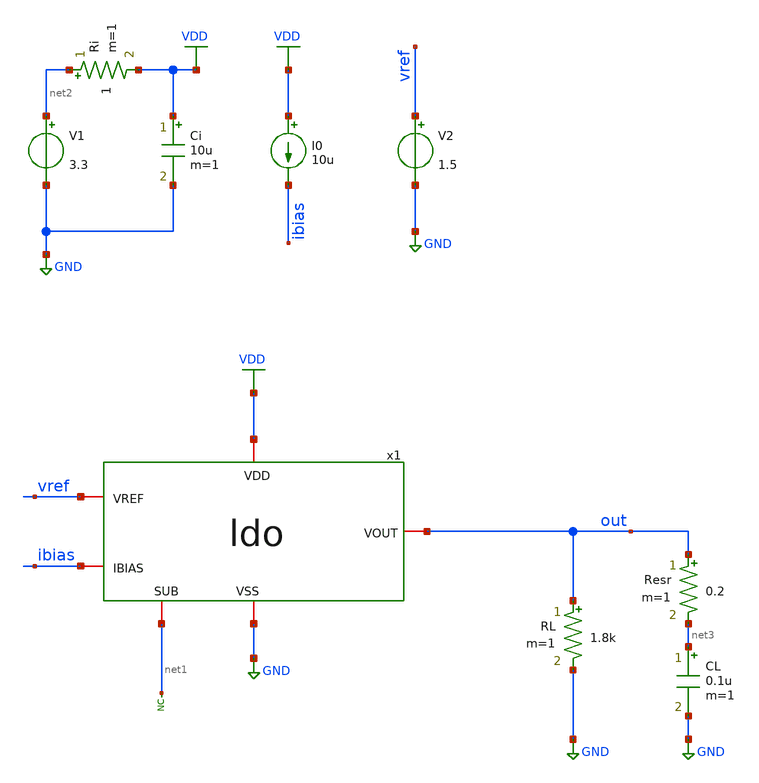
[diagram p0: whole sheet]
** sch_path: designs/libs/tb_ldo/tb_ldo/tb_ldo/tb_ldo_psrr/tb_ldo_psrr.sch
**.subckt tb_ldo_psrr
* noconn #net1
RL out GND 1.8k m=1
V1 net2 GND 3.3
V2 vref GND 1.5
I0 VDD ibias 10u
CL net3 GND 0.1u m=1
Resr out net3 0.2 m=1
x1 VDD vref out ibias net1 GND ldo
Ri net2 VDD 1 m=1
Ci VDD GND 10u m=1
**** begin user architecture code



.control
save all

** Set sources
alter @V1[AC] = 1

** Simulations
ac dec 100 1 10G

** Plots
setplot ac1
let vout = v(out)
let psrr_db = db(vout)
plot psrr_db

** Measurements
meas ac PSRR_gain FIND psrr_db AT=1Hz
let psrr_3db = PSRR_gain+3
meas ac f_3db WHEN psrr_db=$&psrr_3db

write tb_ldo_psrr.raw

.endc
* ngspice commands




.include $::180MCU_MODELS/design.ngspice
.lib $::180MCU_MODELS/sm141064.ngspice typical
.lib $::180MCU_MODELS/sm141064.ngspice cap_mim
.lib $::180MCU_MODELS/sm141064.ngspice moscap_typical
.lib $::180MCU_MODELS/sm141064.ngspice mimcap_typical
.lib $::180MCU_MODELS/sm141064.ngspice res_typical
* .lib $::180MCU_MODELS/sm141064.ngspice res_statistical
* ngspice commands

**** end user architecture code
**.ends
.GLOBAL GND
.GLOBAL VDD
.end
